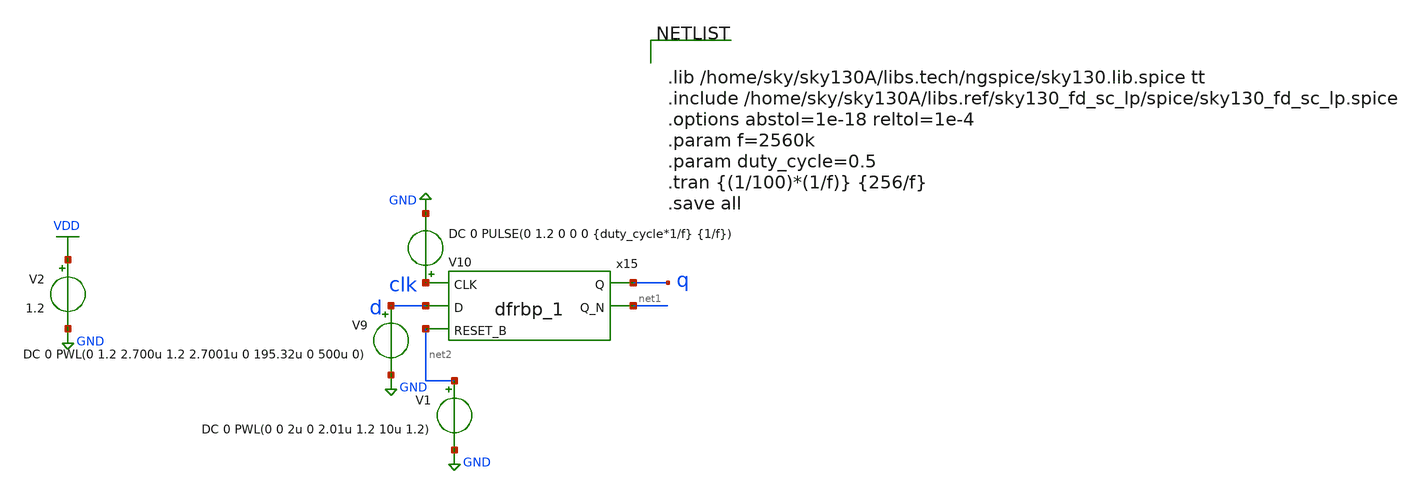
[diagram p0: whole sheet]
** sch_path: xschem/D_flip_flop/untitled-7.sch
**.subckt untitled-7
x15 clk d net2 gnd gnd vdd vdd q net1 sky130_fd_sc_lp__dfrbp_1
V10 clk GND DC 0 PULSE(0 1.2 0 0 0 {duty_cycle*1/f} {1/f})
V9 d GND DC 0 PWL(0 1.2 2.700u 1.2 2.7001u 0 195.32u 0 500u 0)
V1 net2 GND DC 0 PWL(0 0 2u 0 2.01u 1.2 10u 1.2)
V2 VDD GND 1.2
**** begin user architecture code


.lib /home/sky/sky130A/libs.tech/ngspice/sky130.lib.spice tt
.include /home/sky/sky130A/libs.ref/sky130_fd_sc_lp/spice/sky130_fd_sc_lp.spice
.options abstol=1e-18 reltol=1e-4
.param f=2560k
.param duty_cycle=0.5
.tran {(1/100)*(1/f)} {256/f}
.save all


**** end user architecture code
**.ends
.GLOBAL GND
.GLOBAL VDD
.end
